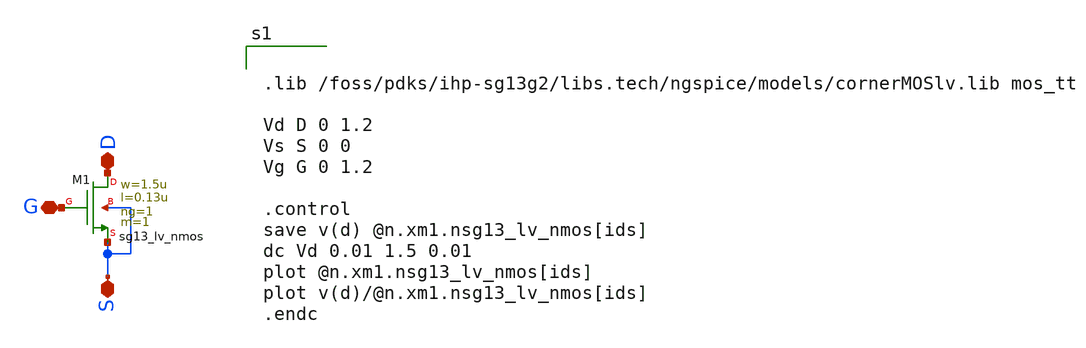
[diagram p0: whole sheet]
** sch_path: xschem/nmos_tb.sch
**.subckt nmos_tb S G D
*.iopin S
*.iopin G
*.iopin D
XM1 D G S S sg13_lv_nmos w=1.5u l=0.13u ng=1 m=1 mm_ok=1
**** begin user architecture code


.lib /foss/pdks/ihp-sg13g2/libs.tech/ngspice/models/cornerMOSlv.lib mos_tt

Vd D 0 1.2
Vs S 0 0
Vg G 0 1.2

.control
save v(d) @n.xm1.nsg13_lv_nmos[ids]
dc Vd 0.01 1.5 0.01
plot @n.xm1.nsg13_lv_nmos[ids]
plot v(d)/@n.xm1.nsg13_lv_nmos[ids]
.endc


**** end user architecture code
**.ends
.end
